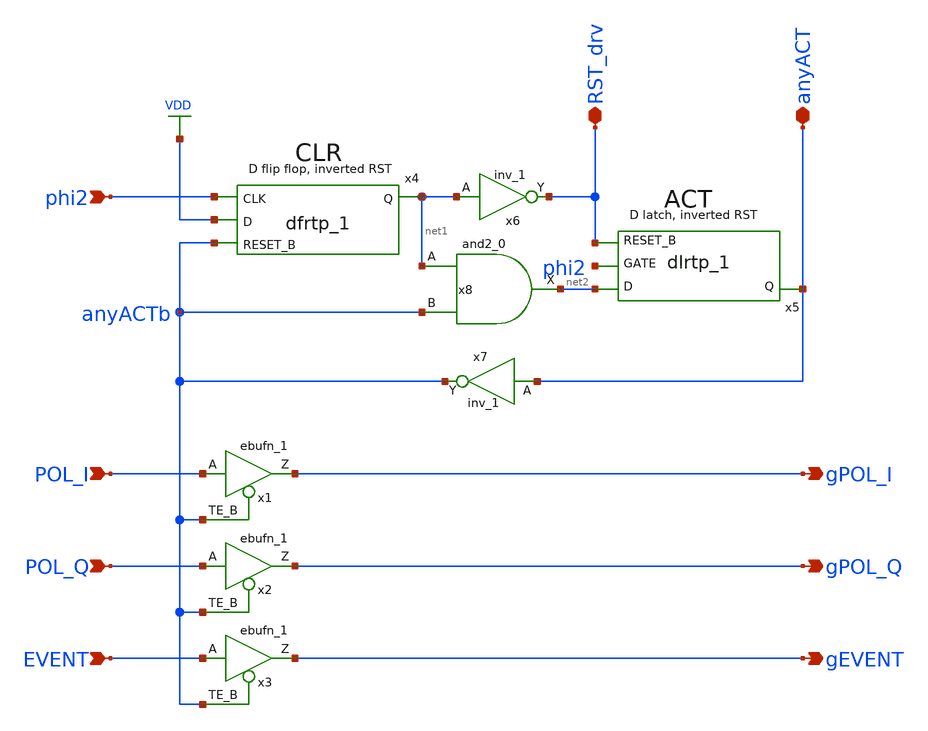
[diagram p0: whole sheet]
** sch_path: xschem/readout/CLR_ACT.sch
**.subckt CLR_ACT POL_I POL_Q EVENT gPOL_I gPOL_Q gEVENT phi2 RST_drv anyACT
*.ipin POL_I
*.ipin POL_Q
*.ipin EVENT
*.opin gPOL_I
*.opin gPOL_Q
*.opin gEVENT
*.ipin phi2
*.iopin RST_drv
*.iopin anyACT
x1 POL_I anyACTb gnd gnd vdd vdd gPOL_I sky130_fd_sc_lp__ebufn_1
x4 phi2 VDD anyACTb gnd gnd vdd vdd net1 sky130_fd_sc_lp__dfrtp_1
x5 net2 phi2 RST_drv gnd gnd vdd vdd anyACT sky130_fd_sc_lp__dlrtp_1
x7 anyACT gnd gnd vdd vdd anyACTb sky130_fd_sc_lp__inv_1
x8 net1 anyACTb gnd gnd vdd vdd net2 sky130_fd_sc_lp__and2_0
x6 net1 gnd gnd vdd vdd RST_drv sky130_fd_sc_lp__inv_1
x2 POL_Q anyACTb gnd gnd vdd vdd gPOL_Q sky130_fd_sc_lp__ebufn_1
x3 EVENT anyACTb gnd gnd vdd vdd gEVENT sky130_fd_sc_lp__ebufn_1
**.ends
.GLOBAL VDD
.end
